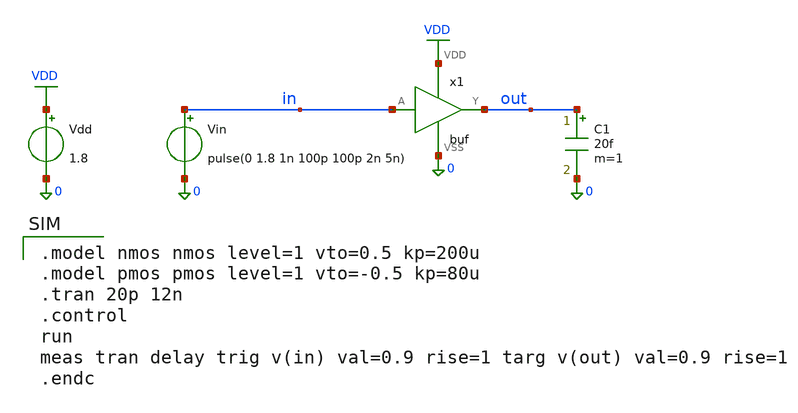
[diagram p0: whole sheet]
** sch_path: examples/buffer/libs/bench/tb_buf/schematic/tb_buf.sch
**.subckt tb_buf
x1 in out VDD 0 buf
Vdd VDD 0 1.8
Vin in 0 pulse(0 1.8 1n 100p 100p 2n 5n)
C1 out 0 20f m=1
**** begin user architecture code

.model nmos nmos level=1 vto=0.5 kp=200u
.model pmos pmos level=1 vto=-0.5 kp=80u
.tran 20p 12n
.control
run
meas tran delay trig v(in) val=0.9 rise=1 targ v(out) val=0.9 rise=1
.endc

**** end user architecture code
**.ends
.GLOBAL VDD
.end
